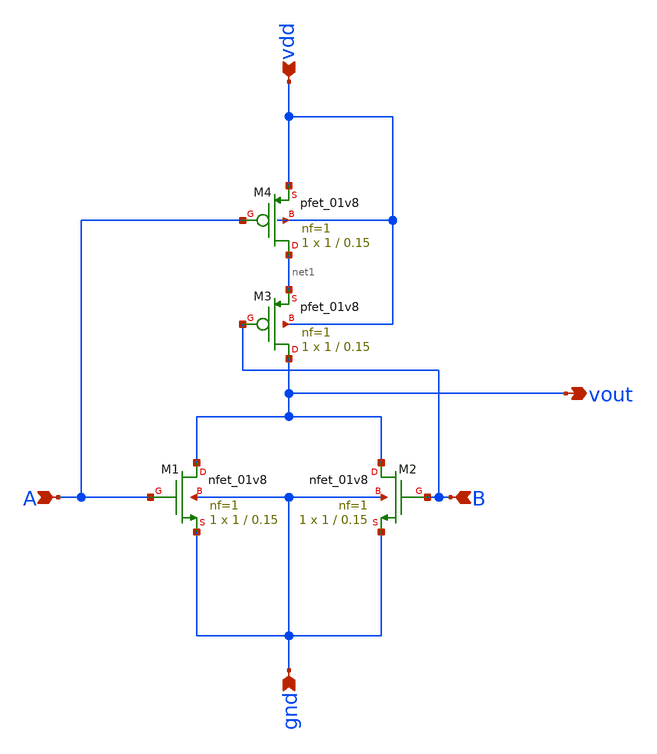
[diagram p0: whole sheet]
** sch_path: nor.sch
**.subckt nor vdd gnd A B vout
*.ipin vdd
*.ipin gnd
*.ipin A
*.ipin B
*.opin vout
XM1 vout A gnd gnd sky130_fd_pr__nfet_01v8 L=0.15 W=1 nf=1 ad='int((nf+1)/2) * W/nf * 0.29' as='int((nf+2)/2) * W/nf * 0.29'
+ pd='2*int((nf+1)/2) * (W/nf + 0.29)' ps='2*int((nf+2)/2) * (W/nf + 0.29)' nrd='0.29 / W' nrs='0.29 / W'
+ sa=0 sb=0 sd=0 mult=1 m=1
XM2 vout B gnd gnd sky130_fd_pr__nfet_01v8 L=0.15 W=1 nf=1 ad='int((nf+1)/2) * W/nf * 0.29' as='int((nf+2)/2) * W/nf * 0.29'
+ pd='2*int((nf+1)/2) * (W/nf + 0.29)' ps='2*int((nf+2)/2) * (W/nf + 0.29)' nrd='0.29 / W' nrs='0.29 / W'
+ sa=0 sb=0 sd=0 mult=1 m=1
XM3 vout B net1 vdd sky130_fd_pr__pfet_01v8 L=0.15 W=1 nf=1 ad='int((nf+1)/2) * W/nf * 0.29' as='int((nf+2)/2) * W/nf * 0.29'
+ pd='2*int((nf+1)/2) * (W/nf + 0.29)' ps='2*int((nf+2)/2) * (W/nf + 0.29)' nrd='0.29 / W' nrs='0.29 / W'
+ sa=0 sb=0 sd=0 mult=1 m=1
XM4 net1 A vdd vdd sky130_fd_pr__pfet_01v8 L=0.15 W=1 nf=1 ad='int((nf+1)/2) * W/nf * 0.29' as='int((nf+2)/2) * W/nf * 0.29'
+ pd='2*int((nf+1)/2) * (W/nf + 0.29)' ps='2*int((nf+2)/2) * (W/nf + 0.29)' nrd='0.29 / W' nrs='0.29 / W'
+ sa=0 sb=0 sd=0 mult=1 m=1
**.ends
.end
